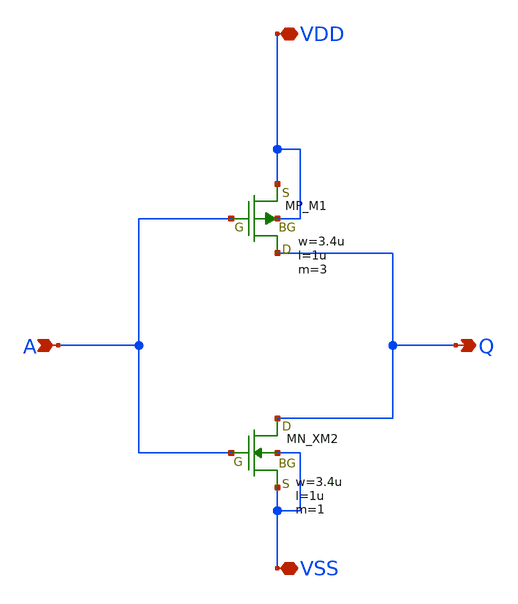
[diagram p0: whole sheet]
** sch_path: member_project/inverter/sanken/pankani/inverter_pankani.sch
**.subckt inverter_pankani VDD VSS A Q
*.iopin VDD
*.iopin VSS
*.ipin A
*.opin Q
XM1 Q A VDD VDD PMOS w=3.4u l=1u nrd=0 nrs=0 m=3
XXM2 Q A VSS VSS NMOS w=3.4u l=1u nrd=0 nrs=0 m=1
**.ends
.end
